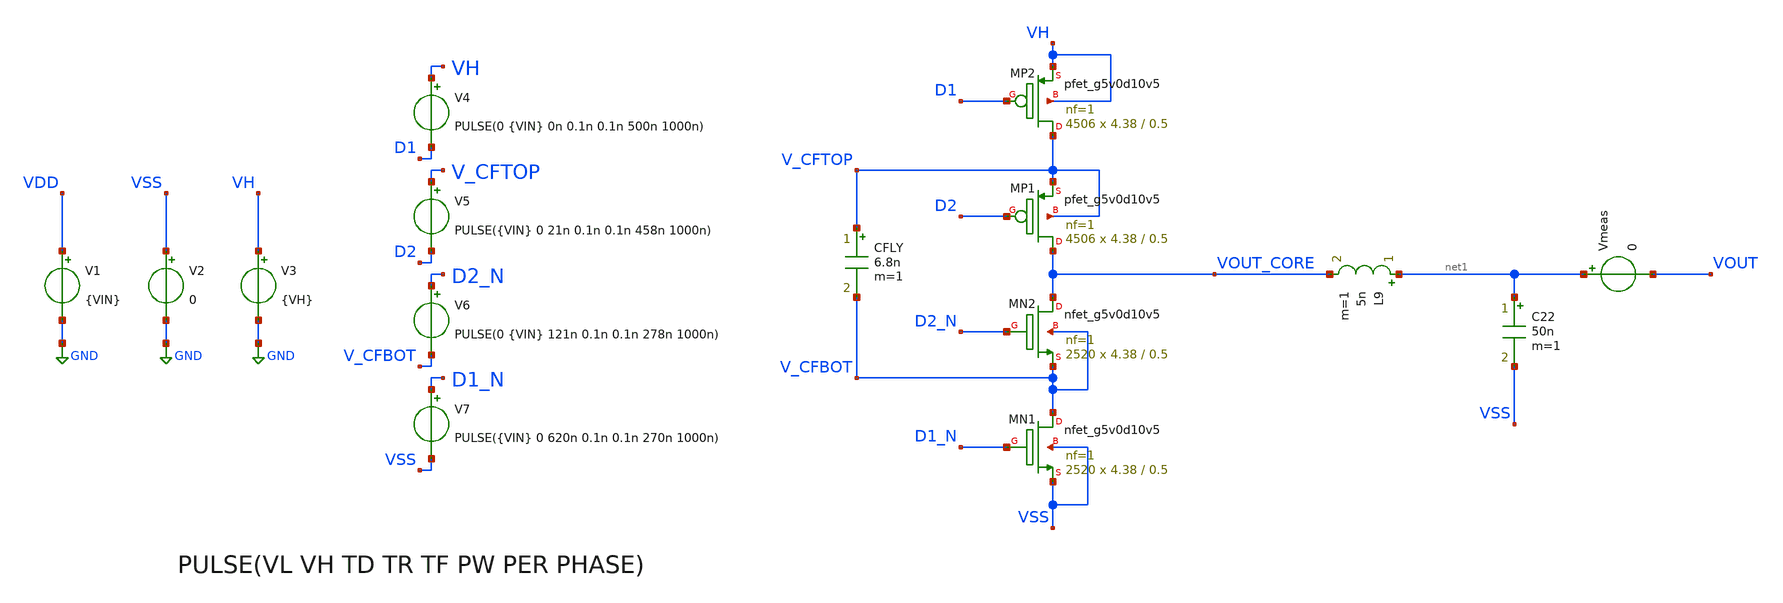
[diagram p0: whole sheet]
** sch_path: xschem/dev_switches/DCDC_5V_FINAL/DCDC_v1p5_1MHz_NMOS_PMOS_sng.sch
**.subckt DCDC_v1p5_1MHz_NMOS_PMOS_sng
XMN2 VOUT_CORE D2_N V_CFBOT V_CFBOT sky130_fd_pr__nfet_g5v0d10v5 L=0.5 W=4.38 nf=1 ad='int((nf+1)/2) * W/nf * 0.29'
+ as='int((nf+2)/2) * W/nf * 0.29' pd='2*int((nf+1)/2) * (W/nf + 0.29)' ps='2*int((nf+2)/2) * (W/nf + 0.29)'
+ nrd='0.29 / W' nrs='0.29 / W' sa=0 sb=0 sd=0 mult=2520 m=2520
XMN1 V_CFBOT D1_N VSS VSS sky130_fd_pr__nfet_g5v0d10v5 L=0.5 W=4.38 nf=1 ad='int((nf+1)/2) * W/nf * 0.29'
+ as='int((nf+2)/2) * W/nf * 0.29' pd='2*int((nf+1)/2) * (W/nf + 0.29)' ps='2*int((nf+2)/2) * (W/nf + 0.29)'
+ nrd='0.29 / W' nrs='0.29 / W' sa=0 sb=0 sd=0 mult=2520 m=2520
CFLY V_CFTOP V_CFBOT 6.8n m=1
V1 VDD GND {VIN}
V4 VH D1 PULSE(0 {VIN} 0n 0.1n 0.1n 500n 1000n)
V2 VSS GND 0
V6 D2_N V_CFBOT PULSE(0 {VIN} 121n 0.1n 0.1n 278n 1000n)
L9 net1 VOUT_CORE 5n m=1
C22 net1 VSS 50n m=1
V3 VH GND {VH}
XMP2 V_CFTOP D1 VH VH sky130_fd_pr__pfet_g5v0d10v5 L=0.5 W=4.38 nf=1 ad='int((nf+1)/2) * W/nf * 0.29'
+ as='int((nf+2)/2) * W/nf * 0.29' pd='2*int((nf+1)/2) * (W/nf + 0.29)' ps='2*int((nf+2)/2) * (W/nf + 0.29)'
+ nrd='0.29 / W' nrs='0.29 / W' sa=0 sb=0 sd=0 mult=4506 m=4506
XMP1 VOUT_CORE D2 V_CFTOP V_CFTOP sky130_fd_pr__pfet_g5v0d10v5 L=0.5 W=4.38 nf=1 ad='int((nf+1)/2) * W/nf * 0.29'
+ as='int((nf+2)/2) * W/nf * 0.29' pd='2*int((nf+1)/2) * (W/nf + 0.29)' ps='2*int((nf+2)/2) * (W/nf + 0.29)'
+ nrd='0.29 / W' nrs='0.29 / W' sa=0 sb=0 sd=0 mult=4506 m=4506
Vmeas net1 VOUT 0
V5 V_CFTOP D2 PULSE({VIN} 0 21n 0.1n 0.1n 458n 1000n)
V7 D1_N VSS PULSE({VIN} 0 620n 0.1n 0.1n 270n 1000n)
**** begin user architecture code


.param VIN = 5
.param VH = 5
.param RL = 50
.option scale=1e-6
*.option temp=70
.ic v(V_CFTOP) = VH/2
.ic v(vout)=0
.ic v(V_CFBOT) = 0
*.probe vd(MP2:G:S)
*.save all
*.save v(d1) v(d2) v(d1top_5v) v(d2_5v) v(d2bot_5v) v(d1bot_5v) v(vout) v(vout_core) v(vdd) v(vh) i(v1) i(v5) i(vmeas) v(v_cftop,v_cfbot)
.save v(D1) v(D2) v(D1_N) v(D2_N) v(VOUT) v(VOUT_CORE) v(vdd) v(vh) i(v1) i(v3) i(vmeas) v(v_cftop,v_cfbot) v(D1,v_cftop) v(D2,vout_core) v(D2_N,v_cfbot) v(D1_Nv,VSS)
.param mc_mm_switch=0
*.lib /home/jorge/Documents/Postdoc/share/pdk/sky130A/libs.tech/ngspice/sky130.lib.spice tt
*.lib /usr/share/pdk/sky130A/libs.tech/ngspice/sky130.lib.spice ss
.lib /foss/pdk/sky130A/libs.tech/ngspice/sky130.lib.spice TT
*.include /usr/share/pdk/sky130A/libs.ref/sky130_fd_sc_hvl/spice/sky130_fd_sc_hvl.spice
*.include /home/jorge/Documents/Postdoc/share/pdk/sky130A/libs.ref/sky130_fd_sc_hvl/spice/sky130_fd_sc_hvl.spice
.options savecurrents
.control
*save all
tran 100n 3u
write DCDC_v1p4_5MHz_NMOS_PMOS.raw
*wrdata
*+ ~/Documents/Postdoc/chipathon2022/3LFCC_AC3E/xschem/dev_switches/DCDC_5V_FINAL/3LFCC_v1p4.txt tran.v(vout) tran.i(vmeas) tran.v(vdd) tran.i(v1) tran.v(vh) tran.i(v5)
wrdata /foss/designs/personal/3LFCC_AC3E/xschem/dev_switches/DCDC_5V_FINAL/3LFCC_v1p4.txt
+ tran.v(vout) tran.i(v3) tran.i(v1)

*plot v(d1top_5v) v(d2_5v)
*plot v(d2bot_5v) v(d1bot_5v)
plot v(v_cftop,v_cfbot) v(vout)
plot v(D1,VH) v(D1_N,VSS)
plot v(D2,V_CFTOP) v(D2_N,V_CFBOT)
plot v(vout) v(vout_core)



*plot v(d1top_5v) v(d2_5v) v(d2bot_5v) v(d1bot_5v) v(v_cftop,v_cfbot) v(vout)
*plot v(v_cftop,v_cfbot) v(vout)
.endc


**** end user architecture code
**.ends
.GLOBAL GND
.end
